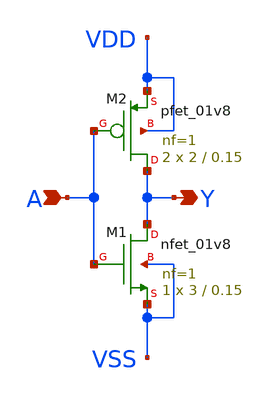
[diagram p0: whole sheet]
** sch_path: archives/lib/xschem/INVX1.sch
**.subckt INVX1 Y A
*.opin Y
*.ipin A
XM1 Y A VSS VSS sky130_fd_pr__nfet_01v8 L=0.15 W=3 nf=1 ad='int((nf+1)/2) * W/nf * 0.29' as='int((nf+2)/2) * W/nf * 0.29'
+ pd='2*int((nf+1)/2) * (W/nf + 0.29)' ps='2*int((nf+2)/2) * (W/nf + 0.29)' nrd='0.29 / W' nrs='0.29 / W'
+ sa=0 sb=0 sd=0 mult=1 m=1
XM2 Y A VDD VDD sky130_fd_pr__pfet_01v8 L=0.15 W=2 nf=1 ad='int((nf+1)/2) * W/nf * 0.29' as='int((nf+2)/2) * W/nf * 0.29'
+ pd='2*int((nf+1)/2) * (W/nf + 0.29)' ps='2*int((nf+2)/2) * (W/nf + 0.29)' nrd='0.29 / W' nrs='0.29 / W'
+ sa=0 sb=0 sd=0 mult=2 m=2
**.ends
.end
